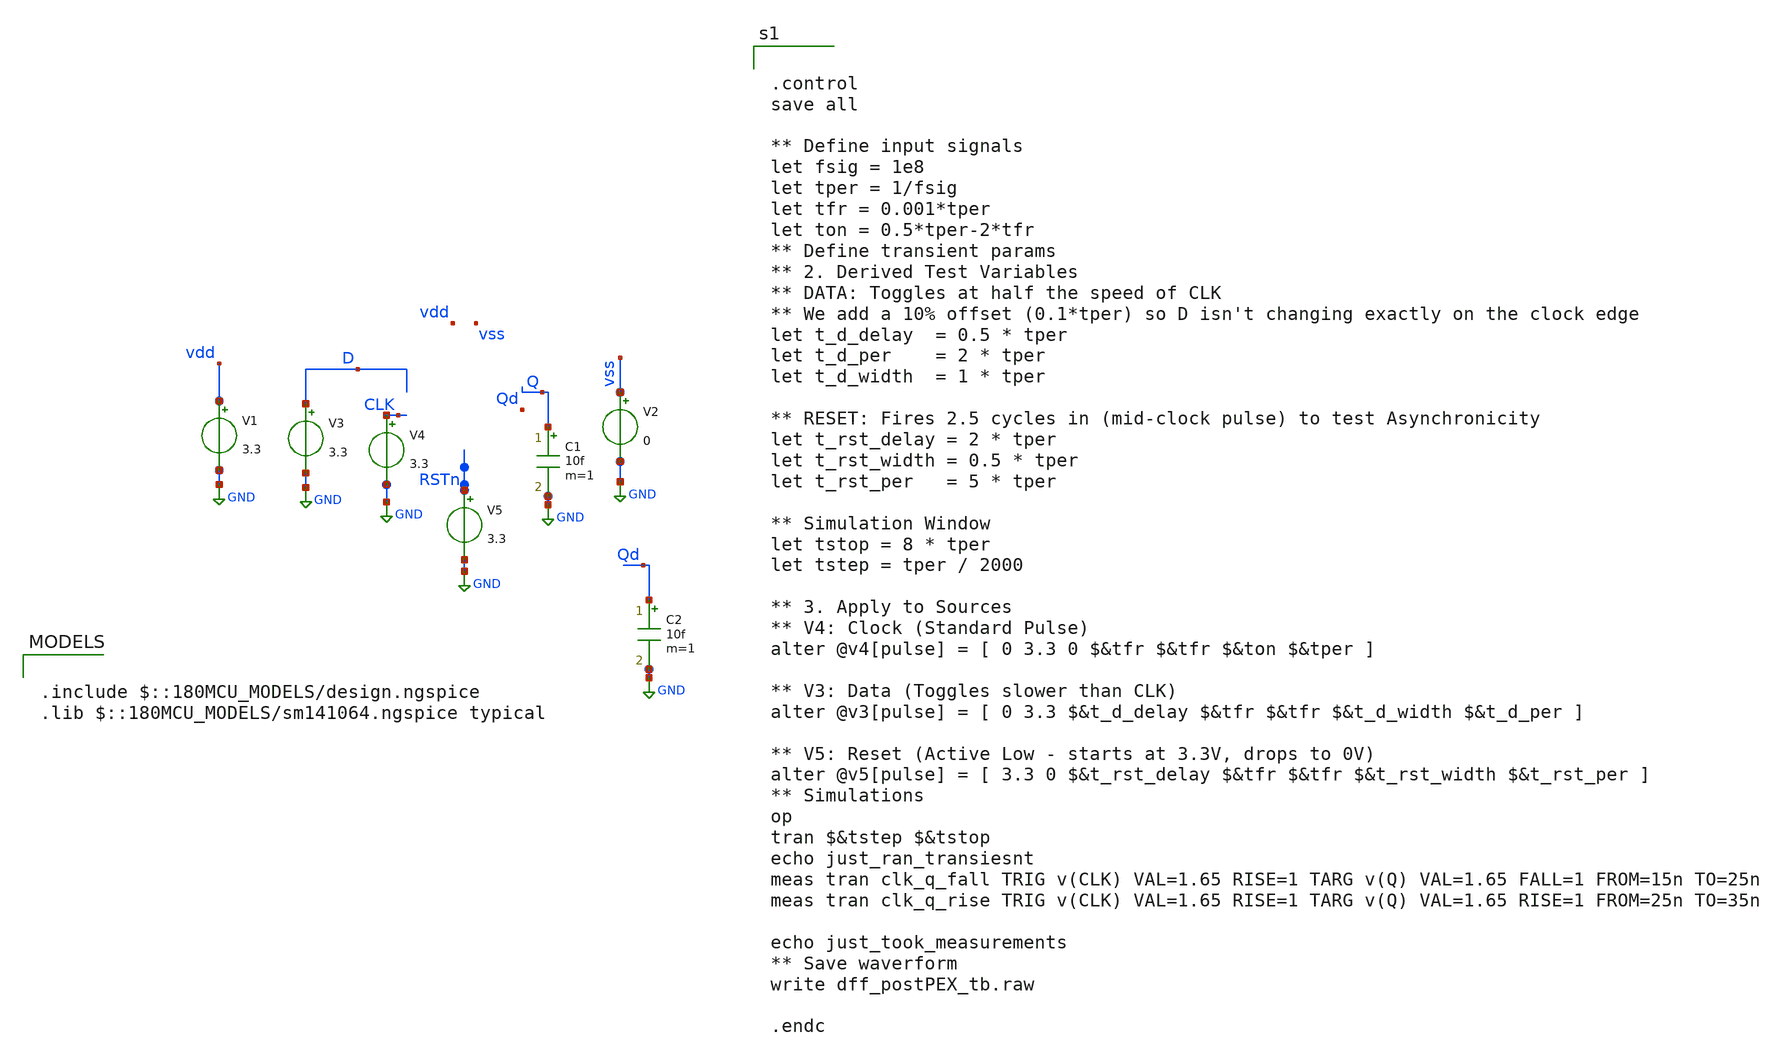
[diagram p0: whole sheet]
** sch_path: schematics/PC/DFF/DFF_postPEX_tb.sch
**.subckt DFF_postPEX_tb
V2 vss GND 0
V1 vdd GND 3.3
V3 D GND 3.3
V4 CLK GND 3.3
V5 RSTn GND 3.3
C1 Q GND 10f m=1
C2 Qd GND 10f m=1
**** begin user architecture code

.include $::180MCU_MODELS/design.ngspice
.lib $::180MCU_MODELS/sm141064.ngspice typical



.control
save all

** Define input signals
let fsig = 1e8
let tper = 1/fsig
let tfr = 0.001*tper
let ton = 0.5*tper-2*tfr
** Define transient params
** 2. Derived Test Variables
** DATA: Toggles at half the speed of CLK
** We add a 10% offset (0.1*tper) so D isn't changing exactly on the clock edge
let t_d_delay  = 0.5 * tper
let t_d_per    = 2 * tper
let t_d_width  = 1 * tper

** RESET: Fires 2.5 cycles in (mid-clock pulse) to test Asynchronicity
let t_rst_delay = 2 * tper
let t_rst_width = 0.5 * tper
let t_rst_per   = 5 * tper

** Simulation Window
let tstop = 8 * tper
let tstep = tper / 2000

** 3. Apply to Sources
** V4: Clock (Standard Pulse)
alter @v4[pulse] = [ 0 3.3 0 $&tfr $&tfr $&ton $&tper ]

** V3: Data (Toggles slower than CLK)
alter @v3[pulse] = [ 0 3.3 $&t_d_delay $&tfr $&tfr $&t_d_width $&t_d_per ]

** V5: Reset (Active Low - starts at 3.3V, drops to 0V)
alter @v5[pulse] = [ 3.3 0 $&t_rst_delay $&tfr $&tfr $&t_rst_width $&t_rst_per ]
** Simulations
op
tran $&tstep $&tstop
echo just_ran_transiesnt
meas tran clk_q_fall TRIG v(CLK) VAL=1.65 RISE=1 TARG v(Q) VAL=1.65 FALL=1 FROM=15n TO=25n
meas tran clk_q_rise TRIG v(CLK) VAL=1.65 RISE=1 TARG v(Q) VAL=1.65 RISE=1 FROM=25n TO=35n

echo just_took_measurements
** Save waverform
write dff_postPEX_tb.raw

.endc






.subckt pfet$1$1 a_52_n92# a_n134_n92# a_146_768# w_n272_n230# a_212_n92# a_n14_768#  VSUBS
X0 a_52_n92# a_n14_768# a_n134_n92# w_n272_n230# pfet_03v3 ad=1.04p pd=4.52u as=2.6p ps=9.3u w=4u l=0.28u
X1 a_212_n92# a_146_768# a_52_n92# w_n272_n230# pfet_03v3 ad=2.6p pd=9.3u as=1.04p ps=4.52u w=4u l=0.28u
C0 a_146_768# a_52_n92# 0.02941f
C1 a_212_n92# w_n272_n230# 0.4912f
C2 a_n14_768# w_n272_n230# 0.12037f
C3 w_n272_n230# a_n134_n92# 0.03964f
C4 w_n272_n230# a_52_n92# 0.00676f
C5 a_n14_768# a_n134_n92# 0.02707f
C6 a_212_n92# a_52_n92# 0.27893f
C7 w_n272_n230# a_146_768# 0.12606f
C8 a_n14_768# a_52_n92# 0.02941f
C9 a_n134_n92# a_52_n92# 0.27893f
C10 a_212_n92# a_146_768# 0.02707f
C11 a_n14_768# a_146_768# 0.06717f
C12 a_212_n92# VSUBS 0.02011f
C13 a_52_n92# VSUBS 0.02011f
C14 a_n134_n92# VSUBS 0.12084f
C15 a_146_768# VSUBS 0.08709f
C16 a_n14_768# VSUBS 0.09278f
C17 w_n272_n230# VSUBS 2.99699f
.ends

.subckt nfet$1$1 a_n126_n92# a_334_n92# a_52_n92# a_148_368# a_n12_368# a_212_n92#
X0 a_52_n92# a_n12_368# a_n126_n92# a_334_n92# nfet_03v3 ad=0.52p pd=2.52u as=1.22p ps=5.22u w=2u l=0.28u
X1 a_212_n92# a_148_368# a_52_n92# a_334_n92# nfet_03v3 ad=1.22p pd=5.22u as=0.52p ps=2.52u w=2u l=0.28u
C0 a_148_368# a_n12_368# 0.0661f
C1 a_n12_368# a_52_n92# 0.01246f
C2 a_148_368# a_52_n92# 0.01246f
C3 a_n12_368# a_n126_n92# 0.01165f
C4 a_148_368# a_212_n92# 0.01165f
C5 a_52_n92# a_212_n92# 0.1173f
C6 a_52_n92# a_n126_n92# 0.1173f
C7 a_212_n92# a_334_n92# 0.2366f
C8 a_52_n92# a_334_n92# 0.02665f
C9 a_n126_n92# a_334_n92# 0.08144f
C10 a_148_368# a_334_n92# 0.21084f
C11 a_n12_368# a_334_n92# 0.21084f
.ends

.subckt TSI vdd cbar c nfet$1$1_0/a_52_n92# m1_222_n517# pfet$1$1_0/a_52_n92# a_99_n1102#  vss
Xpfet$1$1_0 pfet$1$1_0/a_52_n92# m1_222_n517# c vdd vdd a_99_n1102# vss pfet$1$1
Xnfet$1$1_0 m1_222_n517# vss nfet$1$1_0/a_52_n92# cbar a_99_n1102# vss nfet$1$1
C0 nfet$1$1_0/a_52_n92# pfet$1$1_0/a_52_n92# 0.00761f
C1 a_99_n1102# m1_222_n517# 0.02722f
C2 cbar pfet$1$1_0/a_52_n92# 0
C3 nfet$1$1_0/a_52_n92# cbar -0
C4 nfet$1$1_0/a_52_n92# c 0
C5 a_99_n1102# vdd 0.00822f
C6 m1_222_n517# pfet$1$1_0/a_52_n92# 0.0303f
C7 cbar c 0.01289f
C8 nfet$1$1_0/a_52_n92# m1_222_n517# 0.01373f
C9 vdd pfet$1$1_0/a_52_n92# 0.01509f
C10 cbar m1_222_n517# 0.0043f
C11 c m1_222_n517# 0.01009f
C12 nfet$1$1_0/a_52_n92# vdd 0.00182f
C13 vdd cbar 0
C14 vdd c 0.00866f
C15 a_99_n1102# pfet$1$1_0/a_52_n92# 0
C16 vdd m1_222_n517# 0.12702f
C17 a_99_n1102# nfet$1$1_0/a_52_n92# 0.00117f
C18 a_99_n1102# c -0
C19 nfet$1$1_0/a_52_n92# vss 0.03385f
C20 m1_222_n517# vss 0.54217f
C21 cbar vss 0.21029f
C22 pfet$1$1_0/a_52_n92# vss 0.02011f
C23 c vss 0.07372f
C24 a_99_n1102# vss 0.38567f
C25 vdd vss 3.2229f
.ends

.subckt nfet$1 a_219_n142# a_n37_n10# a_105_n10# a_283_n10#
X0 a_283_n10# a_219_n142# a_105_n10# a_n37_n10# nfet_03v3 ad=0.61p pd=3.22u as=0.61p ps=3.22u w=1u l=0.28u
C0 a_105_n10# a_219_n142# 0.00355f
C1 a_283_n10# a_105_n10# 0.02606f
C2 a_283_n10# a_219_n142# 0.00355f
C3 a_283_n10# a_n37_n10# 0.04141f
C4 a_105_n10# a_n37_n10# 0.08353f
C5 a_219_n142# a_n37_n10# 0.24905f
.ends

.subckt pfet$1 a_n97_10# a_n283_10# a_n163_n126# w_n567_n128# VSUBS
X0 a_n97_10# a_n163_n126# a_n283_10# w_n567_n128# pfet_03v3 ad=1.3p pd=5.3u as=1.3p ps=5.3u w=2u l=0.28u
C0 a_n163_n126# w_n567_n128# 0.14368f
C1 a_n97_10# a_n283_10# 0.09167f
C2 a_n283_10# a_n163_n126# 0.0115f
C3 a_n283_10# w_n567_n128# 0.20387f
C4 a_n97_10# a_n163_n126# 0.0115f
C5 a_n97_10# w_n567_n128# 0.02009f
C6 a_n97_10# VSUBS 0.06093f
C7 a_n283_10# VSUBS 0.01994f
C8 a_n163_n126# VSUBS 0.10833f
C9 w_n567_n128# VSUBS 1.54634f
.ends

.subckt TG c cbar m1_125_152# m1_343_154# vdd vss
Xnfet$1_0 c vss m1_125_152# m1_343_154# nfet$1
Xpfet$1_0 m1_125_152# m1_343_154# cbar vdd vss pfet$1
C0 m1_125_152# vdd 0.02248f
C1 m1_343_154# cbar 0.00523f
C2 cbar vdd 0.00482f
C3 m1_125_152# c 0.00301f
C4 cbar c 0.01051f
C5 m1_343_154# vdd 0.13373f
C6 m1_125_152# cbar 0.0052f
C7 m1_343_154# c 0.00294f
C8 vdd c 0.00507f
C9 m1_125_152# m1_343_154# 0.1874f
C10 m1_125_152# vss 0.28809f
C11 m1_343_154# vss 0.1423f
C12 cbar vss 0.09859f
C13 vdd vss 1.88283f
C14 c vss 0.23754f
.ends

.subckt pfet w_n547_n318# a_n223_n180# a_n289_80# a_n409_n180# VSUBS
X0 a_n223_n180# a_n289_80# a_n409_n180# w_n547_n318# pfet_03v3 ad=0.65p pd=3.3u as=0.65p ps=3.3u w=1u l=0.28u
C0 a_n289_80# a_n223_n180# 0.00351f
C1 w_n547_n318# a_n223_n180# 0.0602f
C2 a_n289_80# w_n547_n318# 0.144f
C3 a_n409_n180# a_n223_n180# 0.02488f
C4 a_n409_n180# a_n289_80# 0.00351f
C5 a_n409_n180# w_n547_n318# 0.01032f
C6 a_n223_n180# VSUBS 0.01985f
C7 a_n409_n180# VSUBS 0.03098f
C8 a_n289_80# VSUBS 0.11038f
C9 w_n547_n318# VSUBS 1.07926f
.ends

.subckt nfet$2 a_n287_80# a_n401_n180# a_n223_n180# a_n101_n180#
X0 a_n223_n180# a_n287_80# a_n401_n180# a_n101_n180# nfet_03v3 ad=0.61p pd=3.22u as=0.61p ps=3.22u w=1u l=0.28u
C0 a_n401_n180# a_n287_80# 0.00355f
C1 a_n223_n180# a_n401_n180# 0.02606f
C2 a_n223_n180# a_n287_80# 0.00355f
C3 a_n223_n180# a_n101_n180# 0.08353f
C4 a_n401_n180# a_n101_n180# 0.04141f
C5 a_n287_80# a_n101_n180# 0.24905f
.ends

.subckt inv vdd a_n604_652# m1_n746_383# vss
Xpfet_0 vdd vdd a_n604_652# m1_n746_383# vss pfet
Xnfet$2_0 a_n604_652# m1_n746_383# vss vss nfet$2
C0 vss m1_n746_383# 0.00819f
C1 vdd vss 0.03701f
C2 vss a_n604_652# 0.00258f
C3 vdd m1_n746_383# 0.04118f
C4 m1_n746_383# a_n604_652# 0.09439f
C5 vdd a_n604_652# 0.04881f
C6 vss 0 0.41298f
C7 m1_n746_383# 0 0.20728f
C8 a_n604_652# 0 0.36751f
C9 vdd 0 1.4305f
.ends

.subckt nfet a_216_0# a_30_260# a_n84_0# a_94_0#
X0 a_94_0# a_30_260# a_n84_0# a_216_0# nfet_03v3 ad=0.61p pd=3.22u as=0.61p ps=3.22u w=1u l=0.28u
C0 a_n84_0# a_30_260# 0.00355f
C1 a_n84_0# a_94_0# 0.02606f
C2 a_30_260# a_94_0# 0.00355f
C3 a_94_0# a_216_0# 0.08353f
C4 a_n84_0# a_216_0# 0.04141f
C5 a_30_260# a_216_0# 0.24905f
.ends

.subckt pfet$1$2 a_254_0# a_n92_0# a_94_0# a_188_260# a_28_260# w_n230_n138# VSUBS
X0 a_254_0# a_188_260# a_94_0# w_n230_n138# pfet_03v3 ad=0.65p pd=3.3u as=0.26p ps=1.52u w=1u l=0.28u
X1 a_94_0# a_28_260# a_n92_0# w_n230_n138# pfet_03v3 ad=0.26p pd=1.52u as=0.65p ps=3.3u w=1u l=0.28u
C0 w_n230_n138# a_94_0# 0.00668f
C1 a_28_260# w_n230_n138# 0.12093f
C2 a_94_0# a_188_260# 0.00377f
C3 a_28_260# a_188_260# 0.06717f
C4 a_28_260# a_94_0# 0.00377f
C5 w_n230_n138# a_n92_0# 0.01032f
C6 w_n230_n138# a_254_0# 0.0602f
C7 a_188_260# a_254_0# 0.00351f
C8 a_94_0# a_n92_0# 0.03081f
C9 w_n230_n138# a_188_260# 0.12662f
C10 a_94_0# a_254_0# 0.03081f
C11 a_28_260# a_n92_0# 0.00351f
C12 a_254_0# VSUBS 0.01985f
C13 a_94_0# VSUBS 0.01985f
C14 a_n92_0# VSUBS 0.03098f
C15 a_188_260# VSUBS 0.09113f
C16 a_28_260# VSUBS 0.09682f
C17 w_n230_n138# VSUBS 1.30774f
.ends

.subckt NAND2 vdd a_n602_n134# m1_n492_n294# m1_n197_176# m1_n402_n170# a_n313_n139#  vss
Xnfet_0 vss a_n313_n139# m1_n402_n170# m1_n492_n294# nfet
Xnfet_1 vss a_n602_n134# m1_n492_n294# vss nfet
Xpfet$1$2_0 vdd m1_n197_176# m1_n402_n170# a_n602_n134# a_n313_n139# vdd vss pfet$1$2
C0 a_n313_n139# m1_n197_176# 0.00461f
C1 a_n602_n134# m1_n492_n294# 0.02726f
C2 m1_n492_n294# m1_n197_176# 0.00806f
C3 a_n602_n134# m1_n197_176# 0.00137f
C4 m1_n402_n170# a_n313_n139# 0.14412f
C5 m1_n402_n170# m1_n492_n294# 0.12486f
C6 m1_n402_n170# a_n602_n134# 0.02286f
C7 m1_n402_n170# m1_n197_176# 0.03988f
C8 a_n313_n139# vdd 0.04067f
C9 m1_n492_n294# vdd 0.01484f
C10 a_n602_n134# vdd 0.03299f
C11 m1_n197_176# vdd 0.11355f
C12 m1_n402_n170# vdd 0.06476f
C13 a_n313_n139# m1_n492_n294# 0.00613f
C14 a_n313_n139# a_n602_n134# 0.02192f
C15 m1_n197_176# vss 0.24635f
C16 a_n602_n134# vss 0.39386f
C17 vdd vss 1.56374f
C18 m1_n492_n294# vss 0.38595f
C19 m1_n402_n170# vss 0.42443f
C20 a_n313_n139# vss 0.46929f
.ends

.subckt DFF vss vdd CLK D RSTn Q Qb
XTSI_0 vdd TG_1/cbar TG_1/c TSI_0/nfet$1$1_0/a_52_n92# m2_1891_n1355# TSI_0/pfet$1$1_0/a_52_n92#  m1_2005_329# vss TSI
XTSI_1 vdd TG_1/cbar TG_1/c TSI_1/nfet$1$1_0/a_52_n92# m1_n1441_369# TSI_1/pfet$1$1_0/a_52_n92#  D vss TSI
XTG_0 TG_1/c TG_1/cbar m2_1891_n1355# m1_661_560# vdd vss TG
Xinv_0 vdd CLK TG_1/cbar vss inv
XTG_1 TG_1/c TG_1/cbar m1_n1441_369# m1_n575_427# vdd vss TG
Xinv_1 vdd TG_1/cbar TG_1/c vss inv
Xinv_2 vdd m1_4064_216# Qb vss inv
Xinv_3 vdd m1_2005_329# m1_4064_216# vss inv
Xinv_4 vdd m1_2005_329# Q vss inv
Xinv_5 vdd m1_n1441_369# m1_661_560# vss inv
XNAND2_1 vdd m1_661_560# NAND2_1/m1_n492_n294# vdd m1_n575_427# RSTn vss NAND2
XNAND2_0 vdd m2_1891_n1355# NAND2_0/m1_n492_n294# vdd m1_2005_329# RSTn vss NAND2
R0 vdd.n12 vdd.n11 11.3351
R1 vdd.n6 vdd 10.8695
R2 vdd vdd 10.3913
R3 vdd.n0 vdd 10.0375
R4 vdd.n9 vdd 10.0364
R5 vdd.n5 vdd 9.99638
R6 vdd.n4 vdd 9.95394
R7 vdd.n6 vdd 9.91179
R8 vdd.n13 vdd.n12 5.56991
R9 vdd.n8 vdd.n7 5.51565
R10 vdd.n2 vdd 5.47828
R11 vdd.n11 vdd.n10 5.05113
R12 vdd.n7 vdd 4.56445
R13 vdd vdd.n13 4.56445
R14 vdd.n3 vdd.n2 4.5005
R15 vdd.n10 vdd 2.719
R16 vdd.n1 vdd 2.719
R17 vdd.n7 vdd 2.51601
R18 vdd vdd.n13 2.51601
R19 vdd.n10 vdd 2.22959
R20 vdd.n1 vdd 2.22959
R21 vdd.n4 vdd.n3 0.882612
R22 vdd.n11 vdd.n9 0.840186
R23 vdd.n3 vdd.n0 0.740065
R24 vdd.n8 vdd.n6 0.679034
R25 vdd.n12 vdd.n5 0.45609
R26 vdd.n9 vdd.n8 0.44673
R27 vdd.n2 vdd.n1 0.433453
R28 vdd.n5 vdd.n4 0.25932
R29 vdd.n0 vdd 0.240873
R30 vss.n38 vss.n37 115985
R31 vss.n38 vss.n13 73479.5
R32 vss.n16 vss.n7 16729.1
R33 vss.n40 vss.n2 14730.2
R34 vss.n2 vss.n0 9374.36
R35 vss.n26 vss.n7 7337.84
R36 vss.n54 vss.n5 6102.08
R37 vss.n55 vss.n3 5111.88
R38 vss.n34 vss.n33 4677.5
R39 vss.n54 vss.n6 4363.43
R40 vss.n9 vss.n3 4199.76
R41 vss.n55 vss.n54 4022.02
R42 vss.n56 vss.n55 4005.88
R43 vss.n39 vss.n0 3907.15
R44 vss.n3 vss.n2 3442.38
R45 vss.n54 vss.n4 3316.43
R46 vss.n40 vss.n39 3233.62
R47 vss.n54 vss.n53 2738.43
R48 vss.n41 vss.n40 2575.45
R49 vss.n56 vss.n2 2441.26
R50 vss.n19 vss.n14 2402.54
R51 vss.n26 vss.n5 2399.88
R52 vss.n37 vss.n35 2292.41
R53 vss.n20 vss.n19 1837.05
R54 vss.n32 vss.n16 1817.65
R55 vss.n39 vss.n38 1785.28
R56 vss.n27 vss.n16 1486.77
R57 vss.n14 vss.n13 1419.13
R58 vss.n41 vss.n8 1270.82
R59 vss.n27 vss.n26 1116.83
R60 vss.n20 vss.n15 1094.33
R61 vss.n53 vss.n7 979.532
R62 vss.n52 vss.n51 777.139
R63 vss.n33 vss.n15 737.313
R64 vss.n33 vss.n32 714.972
R65 vss.n52 vss.n8 658.016
R66 vss.n19 vss.n18 615.226
R67 vss.n35 vss.n14 369.978
R68 vss.n35 vss.n34 260.613
R69 vss.n51 vss.n48 124.808
R70 vss.n34 vss.n8 87.0751
R71 vss.n53 vss.n52 64.9007
R72 vss.n51 vss.n50 15.5018
R73 vss.n51 vss.n49 12.6218
R74 vss.n45 vss.n4 10.5559
R75 vss.n13 vss.n12 10.4905
R76 vss.n28 vss.n27 10.4905
R77 vss.n57 vss.n56 10.4905
R78 vss.n37 vss.n36 10.4905
R79 vss.n59 vss.n0 10.4905
R80 vss.n23 vss.n15 10.4775
R81 vss.n48 vss.n47 10.4775
R82 vss.n21 vss.n20 10.4017
R83 vss.n44 vss.n9 10.4017
R84 vss.n32 vss.n31 10.4005
R85 vss vss.n57 10.1415
R86 vss.n31 vss.n30 10.0655
R87 vss.n24 vss.n23 10.023
R88 vss.n22 vss.n21 9.95612
R89 vss.n47 vss.n46 9.90158
R90 vss.n45 vss.n44 9.84084
R91 vss.n29 vss.n28 9.79025
R92 vss.n18 vss.n17 9.7565
R93 vss.n59 vss.n58 9.7475
R94 vss.n36 vss.n10 9.64625
R95 vss.n12 vss.n11 9.63163
R96 vss.n58 vss.n1 7.86984
R97 vss.n29 vss.n25 7.04445
R98 vss.n43 vss.n42 6.14878
R99 vss.n17 vss.n1 6.04823
R100 vss.n11 vss.n1 5.05691
R101 vss.n42 vss.n41 3.47281
R102 vss.n25 vss.n5 3.47281
R103 vss.n48 vss.n9 3.32871
R104 vss.n30 vss.n29 0.711696
R105 vss.n46 vss.n43 0.675969
R106 vss.n22 vss.n17 0.66963
R107 vss.n58 vss 0.656971
R108 vss.n43 vss.n10 0.627219
R109 vss.n11 vss.n10 0.49175
R110 vss.n30 vss.n24 0.397674
R111 vss.n24 vss.n22 0.240663
R112 vss.n46 vss.n45 0.235344
R113 vss.n42 vss 0.0172494
R114 vss.n25 vss 0.0172494
R115 vss.n21 vss 0.00523684
R116 vss.n44 vss 0.00523684
R117 vss.n12 vss 0.003
R118 vss.n28 vss 0.003
R119 vss.n57 vss 0.003
R120 vss.n18 vss 0.003
R121 vss.n36 vss 0.003
R122 vss vss.n59 0.003
R123 vss.n23 vss 0.00286842
R124 vss.n47 vss 0.00286842
R125 vss.n4 vss 0.00286842
R126 vss.n31 vss 0.00286842
R127 D.n0 D.t0 63.6148
R128 D.n0 D.t1 53.7069
R129 D D.n0 8.00524
R130 CLK.n0 CLK.t0 47.2188
R131 CLK.n0 CLK.t1 24.5076
R132 CLK CLK.n0 8.00524
R133 RSTn.t0 RSTn.t1 85.3215
R134 RSTn.n0 RSTn.t2 60.8144
R135 RSTn.n1 RSTn.t0 57.8117
R136 RSTn.n0 RSTn.t3 24.5076
R137 RSTn.n1 RSTn.n0 8.0005
R138 RSTn RSTn.n1 0.00642105
C0 Qb m1_4064_216# 0.0391f
C1 TG_1/c vss 1.87378f
C2 TG_1/cbar TG_1/c 2.78164f
C3 D vss 0.03301f
C4 TSI_0/nfet$1$1_0/a_52_n92# TSI_0/pfet$1$1_0/a_52_n92# -0.00761f
C5 m2_1891_n1355# TSI_0/nfet$1$1_0/a_52_n92# 0
C6 TG_1/cbar D 0.00307f
C7 m1_2005_329# Q 0.04214f
C8 TG_1/c D 0.00102f
C9 TSI_1/pfet$1$1_0/a_52_n92# vdd 0.01547f
C10 m1_2005_329# m1_n575_427# 0.0026f
C11 Q NAND2_0/m1_n492_n294# 0
C12 vdd CLK 0.00146f
C13 m1_2005_329# vss 0.74648f
C14 vdd Q 0
C15 m1_2005_329# TG_1/cbar 0.36684f
C16 m1_n1441_369# TSI_1/nfet$1$1_0/a_52_n92# 0
C17 NAND2_0/m1_n492_n294# vss 0.01386f
C18 vdd m1_n575_427# 0.15422f
C19 RSTn Q 0.00338f
C20 RSTn m1_n575_427# 0.00846f
C21 vdd vss 0.08045f
C22 m1_661_560# m1_n575_427# 0.03413f
C23 m1_2005_329# TG_1/c 0.08374f
C24 TG_1/cbar vdd 2.87034f
C25 RSTn vss 2.74442f
C26 m1_661_560# vss 0.47901f
C27 TG_1/c NAND2_0/m1_n492_n294# 0.00181f
C28 NAND2_1/m1_n492_n294# m1_n575_427# 0
C29 RSTn TG_1/cbar 0.04508f
C30 m1_661_560# TG_1/cbar 0.20708f
C31 vdd TG_1/c 3.87824f
C32 NAND2_1/m1_n492_n294# vss 0.01665f
C33 NAND2_1/m1_n492_n294# TG_1/cbar 0
C34 RSTn TG_1/c 0.0365f
C35 vdd D 0.011f
C36 m1_661_560# TG_1/c 0.00366f
C37 m1_n1441_369# TSI_1/pfet$1$1_0/a_52_n92# 0
C38 m2_1891_n1355# m1_n575_427# 0
C39 m1_661_560# D 0.00194f
C40 NAND2_1/m1_n492_n294# TG_1/c 0.00287f
C41 m2_1891_n1355# vss 0.27461f
C42 TG_1/cbar TSI_0/pfet$1$1_0/a_52_n92# 0
C43 TG_1/cbar m2_1891_n1355# 1.08018f
C44 Qb vss 0.01912f
C45 m1_n1441_369# m1_n575_427# 0.01076f
C46 m1_2005_329# NAND2_0/m1_n492_n294# 0.0107f
C47 m1_n1441_369# vss 1.12465f
C48 TG_1/c TSI_0/pfet$1$1_0/a_52_n92# 0.07207f
C49 m1_2005_329# vdd 1.16206f
C50 TG_1/c m2_1891_n1355# 0.15856f
C51 m1_n1441_369# TG_1/cbar 0.30044f
C52 RSTn m1_2005_329# 0.81313f
C53 vdd NAND2_0/m1_n492_n294# -0.00238f
C54 m1_661_560# m1_2005_329# 0.00425f
C55 RSTn NAND2_0/m1_n492_n294# 0.0054f
C56 m1_n1441_369# TG_1/c 0.01917f
C57 m1_4064_216# vss 0.16434f
C58 m1_661_560# NAND2_0/m1_n492_n294# 0
C59 m1_2005_329# NAND2_1/m1_n492_n294# 0
C60 TG_1/cbar m1_4064_216# 0.00217f
C61 m1_n1441_369# D 0.01536f
C62 RSTn vdd 2.60302f
C63 m1_661_560# vdd 0.70424f
C64 RSTn m1_661_560# 0.0573f
C65 m1_2005_329# TSI_0/pfet$1$1_0/a_52_n92# 0.01485f
C66 NAND2_1/m1_n492_n294# vdd 0.00307f
C67 m1_2005_329# m2_1891_n1355# 0.16371f
C68 TSI_0/nfet$1$1_0/a_52_n92# vss 0.01228f
C69 TG_1/cbar TSI_0/nfet$1$1_0/a_52_n92# 0
C70 RSTn NAND2_1/m1_n492_n294# 0.00192f
C71 m1_2005_329# Qb 0
C72 m1_661_560# NAND2_1/m1_n492_n294# 0.01109f
C73 m2_1891_n1355# NAND2_0/m1_n492_n294# 0.00997f
C74 TSI_1/nfet$1$1_0/a_52_n92# vss 0.01228f
C75 vdd TSI_0/pfet$1$1_0/a_52_n92# 0.00682f
C76 vdd m2_1891_n1355# 0.28031f
C77 TG_1/c TSI_0/nfet$1$1_0/a_52_n92# -0
C78 TG_1/cbar TSI_1/nfet$1$1_0/a_52_n92# 0
C79 Qb vdd 0.00101f
C80 RSTn m2_1891_n1355# 0.04299f
C81 m1_661_560# TSI_0/pfet$1$1_0/a_52_n92# 0
C82 m1_661_560# m2_1891_n1355# 0.01606f
C83 TSI_1/nfet$1$1_0/a_52_n92# TG_1/c 0
C84 m1_n1441_369# vdd 1.12328f
C85 m1_2005_329# m1_4064_216# 0.03389f
C86 NAND2_1/m1_n492_n294# m2_1891_n1355# 0
C87 RSTn m1_n1441_369# 0.04618f
C88 m1_n1441_369# m1_661_560# 0.03717f
C89 vdd m1_4064_216# 0.1274f
C90 m1_n1441_369# NAND2_1/m1_n492_n294# 0
C91 TSI_1/pfet$1$1_0/a_52_n92# vss 0
C92 m2_1891_n1355# TSI_0/pfet$1$1_0/a_52_n92# 0
C93 m1_2005_329# TSI_0/nfet$1$1_0/a_52_n92# 0.02416f
C94 CLK vss 0.0064f
C95 TG_1/cbar TSI_1/pfet$1$1_0/a_52_n92# 0
C96 RSTn m1_4064_216# 0
C97 TG_1/cbar CLK 0.0471f
C98 Q vss 0.01892f
C99 m1_n1441_369# m2_1891_n1355# 0
C100 m1_n575_427# vss 0.02451f
C101 vdd TSI_0/nfet$1$1_0/a_52_n92# -0.00182f
C102 TG_1/c CLK 0
C103 TG_1/cbar m1_n575_427# 0.01089f
C104 m1_661_560# TSI_0/nfet$1$1_0/a_52_n92# 0
C105 TG_1/cbar vss 1.17633f
C106 TSI_1/nfet$1$1_0/a_52_n92# vdd 0
C107 TG_1/c m1_n575_427# 0.2739f
C108 RSTn.t1 0 0.08747f
C109 RSTn.t0 0 0.61761f
C110 RSTn.t3 0 0.03319f
C111 RSTn.t2 0 0.10218f
C112 RSTn.n0 0 0.10137f
C113 RSTn.n1 0 1.9464f
C114 vdd.n0 0 -0.79026f
C115 vdd.n1 0 -0.20771f
C116 vdd.n2 0 -0.38038f
C117 vdd.n3 0 -1.01222f
C118 vdd.n4 0 -0.86865f
C119 vdd.n5 0 -0.72335f
C120 vdd.n6 0 -2.55491f
C121 vdd.n7 0 -0.24124f
C122 vdd.n8 0 -1.01419f
C123 vdd.n9 0 -1.30826f
C124 vdd.n10 0 -0.33616f
C125 vdd.n11 0 -2.59435f
C126 vdd.n12 0 -2.48061f
C127 vdd.n13 0 -0.24127f
C128 NAND2_0/m1_n492_n294# 0 0.24685f
C129 m1_2005_329# 0 2.63135f
C130 RSTn 0 1.76414f
C131 NAND2_1/m1_n492_n294# 0 0.24685f
C132 m1_n575_427# 0 0.39826f
C133 vss 0 12.29504f
C134 m1_661_560# 0 1.2064f
C135 m1_n1441_369# 0 1.99905f
C136 vdd 0 49.09492f
C137 Q 0 0.18103f
C138 Qb 0 0.178f
C139 m1_4064_216# 0 0.68639f
C140 CLK 0 0.34953f
C141 m2_1891_n1355# 0 1.1088f
C142 TG_1/cbar 0 5.00165f
C143 TSI_1/nfet$1$1_0/a_52_n92# 0 0.02665f
C144 TSI_1/pfet$1$1_0/a_52_n92# 0 0.02011f
C145 TG_1/c 0 8.29951f
C146 D 0 0.3602f
C147 TSI_0/nfet$1$1_0/a_52_n92# 0 0.02665f
C148 TSI_0/pfet$1$1_0/a_52_n92# 0 0.02011f
.ends

X0 vss vdd CLK D RSTn Q Qb DFF



**** end user architecture code
**.ends
.GLOBAL GND
.end
